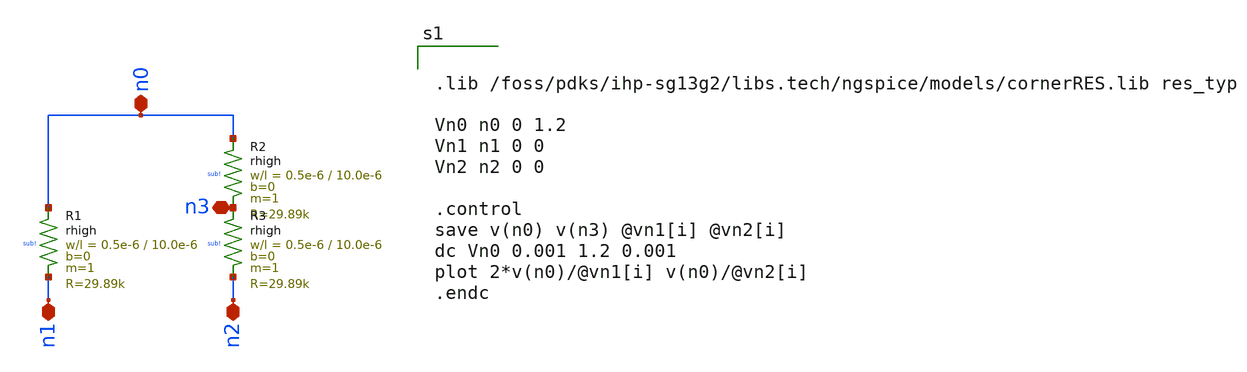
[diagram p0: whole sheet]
** sch_path: xschem/rhigh_tb.sch
**.subckt rhigh_tb n0 n1 n3 n2
*.iopin n0
*.iopin n1
*.iopin n3
*.iopin n2
XR1 n0 n1 sub! rhigh w=0.5e-6 l=10.0e-6 m=1 b=0 mm_ok=1
XR2 n0 n3 sub! rhigh w=0.5e-6 l=10.0e-6 m=1 b=0 mm_ok=1
XR3 n3 n2 sub! rhigh w=0.5e-6 l=10.0e-6 m=1 b=0 mm_ok=1
**** begin user architecture code


.lib /foss/pdks/ihp-sg13g2/libs.tech/ngspice/models/cornerRES.lib res_typ

Vn0 n0 0 1.2
Vn1 n1 0 0
Vn2 n2 0 0

.control
save v(n0) v(n3) @vn1[i] @vn2[i]
dc Vn0 0.001 1.2 0.001
plot 2*v(n0)/@vn1[i] v(n0)/@vn2[i]
.endc


**** end user architecture code
**.ends
.end
